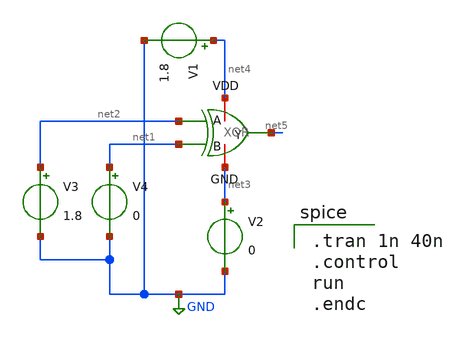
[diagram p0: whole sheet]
** sch_path: FinalProj/XOR_Test.sch
**.subckt XOR_Test
V1 net4 GND 1.8
V2 net3 GND 0
V3 net2 GND 1.8
V4 net1 GND 0
x1 net4 net2 net1 net5 net3 XOR
**** begin user architecture code
 .lib $::SKYWATER_MODELS/sky130.lib.spice tt

.tran 1n 40n
.control
run
.endc

**** end user architecture code
**.ends

* expanding   symbol:  workspace/FinalProj/XOR.sym # of pins=5
** sym_path: FinalProj/XOR.sym
** sch_path: FinalProj/XOR.sch
.subckt XOR VDD A B Y GND
*.ipin A
*.ipin B
*.iopin VDD
*.iopin GND
*.opin Y
x1 VDD B net1 A GND NOR
x2 VDD net2 Y net1 GND NOR
x3 VDD B net2 A GND AND
.ends


* expanding   symbol:  workspace/FinalProj/NOR.sym # of pins=5
** sym_path: FinalProj/NOR.sym
** sch_path: FinalProj/NOR.sch
.subckt NOR VDD B Y A GND
*.ipin B
*.ipin A
*.iopin GND
*.iopin VDD
*.opin Y
XM1 net1 A VDD VDD sky130_fd_pr__pfet_01v8 L=0.5 W=2 nf=1 ad='int((nf+1)/2) * W/nf * 0.29' as='int((nf+2)/2) * W/nf * 0.29'
+ pd='2*int((nf+1)/2) * (W/nf + 0.29)' ps='2*int((nf+2)/2) * (W/nf + 0.29)' nrd='0.29 / W' nrs='0.29 / W'
+ sa=0 sb=0 sd=0 mult=1 m=1
XM2 Y B net1 VDD sky130_fd_pr__pfet_01v8 L=0.5 W=2 nf=1 ad='int((nf+1)/2) * W/nf * 0.29' as='int((nf+2)/2) * W/nf * 0.29'
+ pd='2*int((nf+1)/2) * (W/nf + 0.29)' ps='2*int((nf+2)/2) * (W/nf + 0.29)' nrd='0.29 / W' nrs='0.29 / W'
+ sa=0 sb=0 sd=0 mult=1 m=1
XM3 Y A GND GND sky130_fd_pr__nfet_01v8 L=0.5 W=0.5 nf=1 ad='int((nf+1)/2) * W/nf * 0.29' as='int((nf+2)/2) * W/nf * 0.29'
+ pd='2*int((nf+1)/2) * (W/nf + 0.29)' ps='2*int((nf+2)/2) * (W/nf + 0.29)' nrd='0.29 / W' nrs='0.29 / W'
+ sa=0 sb=0 sd=0 mult=1 m=1
XM4 Y B GND GND sky130_fd_pr__nfet_01v8 L=0.5 W=0.5 nf=1 ad='int((nf+1)/2) * W/nf * 0.29' as='int((nf+2)/2) * W/nf * 0.29'
+ pd='2*int((nf+1)/2) * (W/nf + 0.29)' ps='2*int((nf+2)/2) * (W/nf + 0.29)' nrd='0.29 / W' nrs='0.29 / W'
+ sa=0 sb=0 sd=0 mult=1 m=1
.ends


* expanding   symbol:  workspace/FinalProj/AND.sym # of pins=5
** sym_path: FinalProj/AND.sym
** sch_path: FinalProj/AND.sch
.subckt AND VDD A Y B GND
*.ipin A
*.ipin B
*.iopin VDD
*.iopin GND
*.opin Y
x1 VDD net1 B A GND NAND
x2 VDD net1 Y GND Inv
.ends


* expanding   symbol:  workspace/FinalProj/NAND.sym # of pins=5
** sym_path: FinalProj/NAND.sym
** sch_path: FinalProj/NAND.sch
.subckt NAND VDD Y B A GND
*.ipin A
*.ipin B
*.iopin VDD
*.iopin GND
*.opin Y
XM1 Y B VDD VDD sky130_fd_pr__pfet_01v8 L=0.5 W=2 nf=1 ad='int((nf+1)/2) * W/nf * 0.29' as='int((nf+2)/2) * W/nf * 0.29'
+ pd='2*int((nf+1)/2) * (W/nf + 0.29)' ps='2*int((nf+2)/2) * (W/nf + 0.29)' nrd='0.29 / W' nrs='0.29 / W'
+ sa=0 sb=0 sd=0 mult=1 m=1
XM2 Y A VDD VDD sky130_fd_pr__pfet_01v8 L=0.5 W=2 nf=1 ad='int((nf+1)/2) * W/nf * 0.29' as='int((nf+2)/2) * W/nf * 0.29'
+ pd='2*int((nf+1)/2) * (W/nf + 0.29)' ps='2*int((nf+2)/2) * (W/nf + 0.29)' nrd='0.29 / W' nrs='0.29 / W'
+ sa=0 sb=0 sd=0 mult=1 m=1
XM3 Y B net1 GND sky130_fd_pr__nfet_01v8 L=0.5 W=2 nf=1 ad='int((nf+1)/2) * W/nf * 0.29' as='int((nf+2)/2) * W/nf * 0.29'
+ pd='2*int((nf+1)/2) * (W/nf + 0.29)' ps='2*int((nf+2)/2) * (W/nf + 0.29)' nrd='0.29 / W' nrs='0.29 / W'
+ sa=0 sb=0 sd=0 mult=1 m=1
XM4 net1 A GND GND sky130_fd_pr__nfet_01v8 L=0.5 W=2 nf=1 ad='int((nf+1)/2) * W/nf * 0.29' as='int((nf+2)/2) * W/nf * 0.29'
+ pd='2*int((nf+1)/2) * (W/nf + 0.29)' ps='2*int((nf+2)/2) * (W/nf + 0.29)' nrd='0.29 / W' nrs='0.29 / W'
+ sa=0 sb=0 sd=0 mult=1 m=1
.ends


* expanding   symbol:  workspace/FinalProj/Inv.sym # of pins=4
** sym_path: FinalProj/Inv.sym
** sch_path: FinalProj/Inv.sch
.subckt Inv VDD A Y GND
*.ipin A
*.iopin GND
*.iopin VDD
*.opin Y
XM1 Y A VDD VDD sky130_fd_pr__pfet_01v8 L=0.5 W=1 nf=1 ad='int((nf+1)/2) * W/nf * 0.29' as='int((nf+2)/2) * W/nf * 0.29'
+ pd='2*int((nf+1)/2) * (W/nf + 0.29)' ps='2*int((nf+2)/2) * (W/nf + 0.29)' nrd='0.29 / W' nrs='0.29 / W'
+ sa=0 sb=0 sd=0 mult=1 m=1
XM2 Y A GND GND sky130_fd_pr__nfet_01v8 L=0.5 W=0.5 nf=1 ad='int((nf+1)/2) * W/nf * 0.29' as='int((nf+2)/2) * W/nf * 0.29'
+ pd='2*int((nf+1)/2) * (W/nf + 0.29)' ps='2*int((nf+2)/2) * (W/nf + 0.29)' nrd='0.29 / W' nrs='0.29 / W'
+ sa=0 sb=0 sd=0 mult=1 m=1
.ends

.GLOBAL GND
.end
